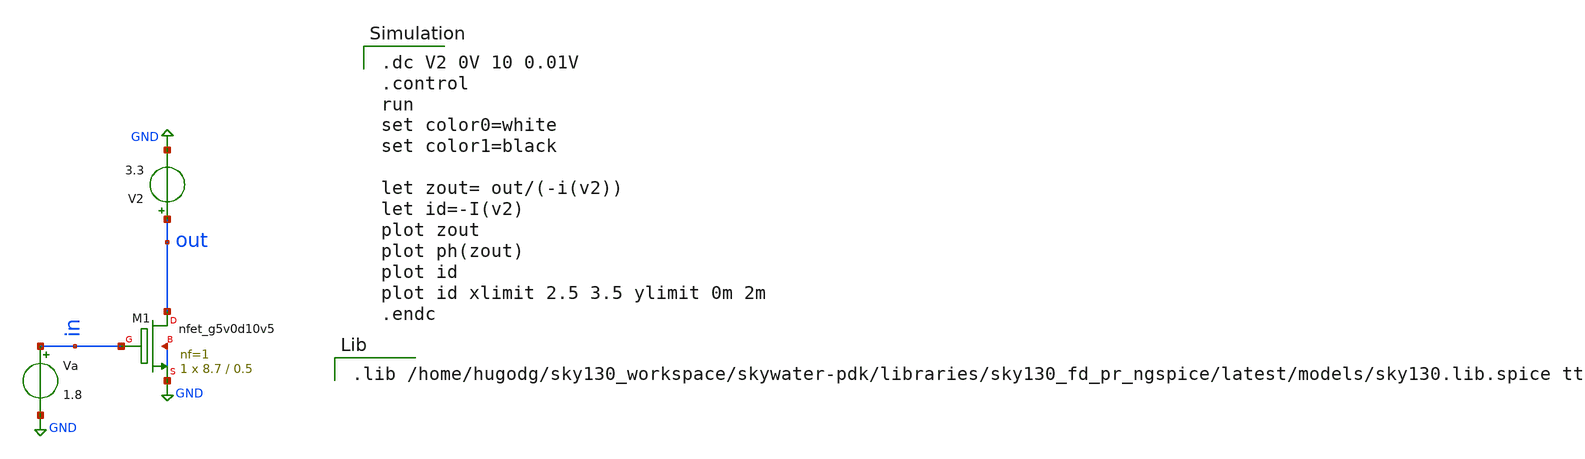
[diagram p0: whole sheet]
** sch_path: ask_modulator/xschem/nmos_tb-dc.sch
**.subckt nmos_tb-dc
Va in GND 1.8
V2 out GND 3.3
XM1 out in GND GND sky130_fd_pr__nfet_g5v0d10v5 L=0.5 W=8.7 nf=1 ad='int((nf+1)/2) * W/nf * 0.29' as='int((nf+2)/2) * W/nf * 0.29'
+ pd='2*int((nf+1)/2) * (W/nf + 0.29)' ps='2*int((nf+2)/2) * (W/nf + 0.29)' nrd='0.29 / W' nrs='0.29 / W'
+ sa=0 sb=0 sd=0 mult=1 m=1
**** begin user architecture code

.dc V2 0V 10 0.01V
.control
run
set color0=white
set color1=black

let zout= out/(-i(v2))
let id=-I(v2)
plot zout
plot ph(zout)
plot id
plot id xlimit 2.5 3.5 ylimit 0m 2m
.endc


.lib /home/hugodg/sky130_workspace/skywater-pdk/libraries/sky130_fd_pr_ngspice/latest/models/sky130.lib.spice tt

**** end user architecture code
**.ends
.GLOBAL GND
.end
